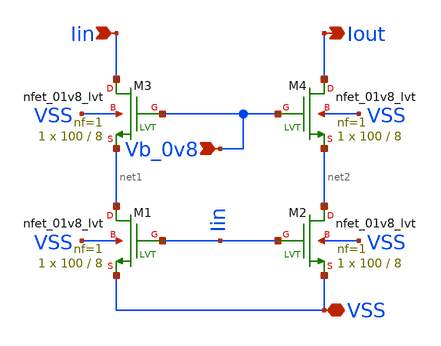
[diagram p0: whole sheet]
** sch_path: wideswing_cur_mir_nmos.sch
**.subckt wideswing_cur_mir_nmos Iin Iout Vb_0v8 VSS
*.ipin Iin
*.opin Iout
*.ipin Vb_0v8
*.iopin VSS
XM1 net1 Iin VSS VSS sky130_fd_pr__nfet_01v8_lvt L=8 W=100 nf=1 ad='int((1 + 1)/2) * 100 / 1 * 0.29'
+ as='int((1 + 2)/2) * 100 / 1 * 0.29' pd='2*int((1 + 1)/2) * (100 / 1 + 0.29)' ps='2*int((1 + 2)/2) * (100 / 1 + 0.29)'
+ nrd='0.29 / 100 ' nrs='0.29 / 100 ' sa=0 sb=0 sd=0 mult=1 m=1
XM2 net2 Iin VSS VSS sky130_fd_pr__nfet_01v8_lvt L=8 W=100 nf=1 ad='int((1 + 1)/2) * 100 / 1 * 0.29'
+ as='int((1 + 2)/2) * 100 / 1 * 0.29' pd='2*int((1 + 1)/2) * (100 / 1 + 0.29)' ps='2*int((1 + 2)/2) * (100 / 1 + 0.29)'
+ nrd='0.29 / 100 ' nrs='0.29 / 100 ' sa=0 sb=0 sd=0 mult=1 m=1
XM3 Iin Vb_0v8 net1 VSS sky130_fd_pr__nfet_01v8_lvt L=8 W=100 nf=1 ad='int((1 + 1)/2) * 100 / 1 * 0.29'
+ as='int((1 + 2)/2) * 100 / 1 * 0.29' pd='2*int((1 + 1)/2) * (100 / 1 + 0.29)' ps='2*int((1 + 2)/2) * (100 / 1 + 0.29)'
+ nrd='0.29 / 100 ' nrs='0.29 / 100 ' sa=0 sb=0 sd=0 mult=1 m=1
XM4 Iout Vb_0v8 net2 VSS sky130_fd_pr__nfet_01v8_lvt L=8 W=100 nf=1 ad='int((1 + 1)/2) * 100 / 1 * 0.29'
+ as='int((1 + 2)/2) * 100 / 1 * 0.29' pd='2*int((1 + 1)/2) * (100 / 1 + 0.29)' ps='2*int((1 + 2)/2) * (100 / 1 + 0.29)'
+ nrd='0.29 / 100 ' nrs='0.29 / 100 ' sa=0 sb=0 sd=0 mult=1 m=1
**.ends
.end
